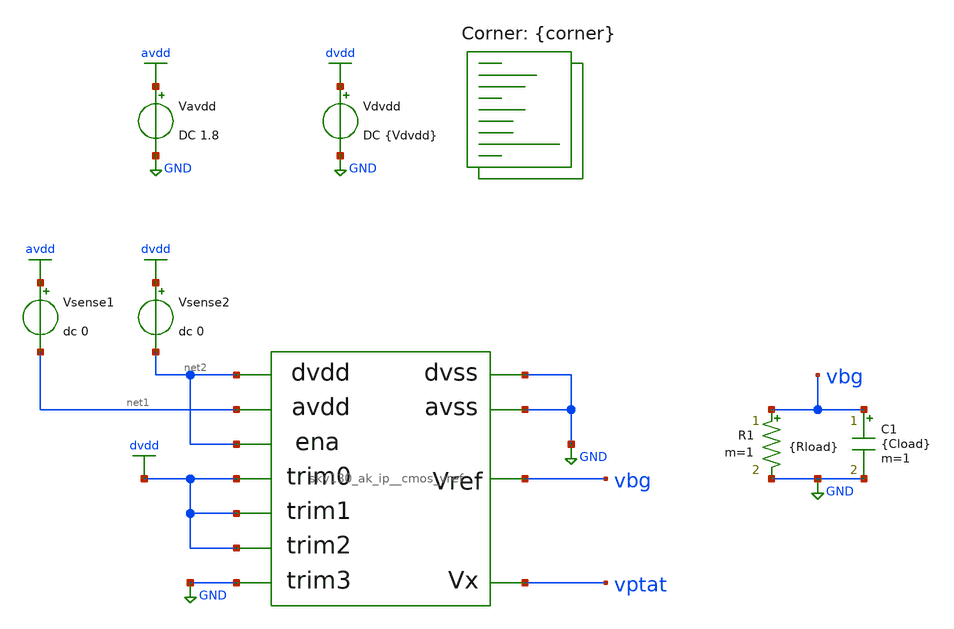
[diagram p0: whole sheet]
** sch_path: cace/tb_supply_sweep.sch
**.subckt tb_supply_sweep
Vavdd avdd GND DC 1.8
X1 net1 GND dvdd vbg vptat dvdd dvdd GND net2 GND net2 sky130_ak_ip__cmos_vref
Vsense1 avdd net1 dc 0
Vdvdd dvdd GND DC {Vdvdd}
C1 vbg GND {Cload} m=1
Vsense2 dvdd net2 dc 0
R1 vbg GND {Rload} m=1
**** begin user architecture code


.option warn=1
.option TEMP={temperature}
.nodeset V(vbg)=1.2
.nodeset V(vptat)=0.2
.control
save vbg
dc Vavdd {Vavdd|minimum} {Vavdd|maximum} 10m
set wr_singlescale
wrdata {simpath}/{filename}_{N}.data V(vbg)
quit
.endc


.lib $::SKYWATER_MODELS/sky130.lib.spice {corner}
 .include $::SKYWATER_STDCELLS/sky130_fd_sc_hd.spice
**** end user architecture code
**.ends
.GLOBAL avdd
.GLOBAL GND
.GLOBAL dvdd
.end
